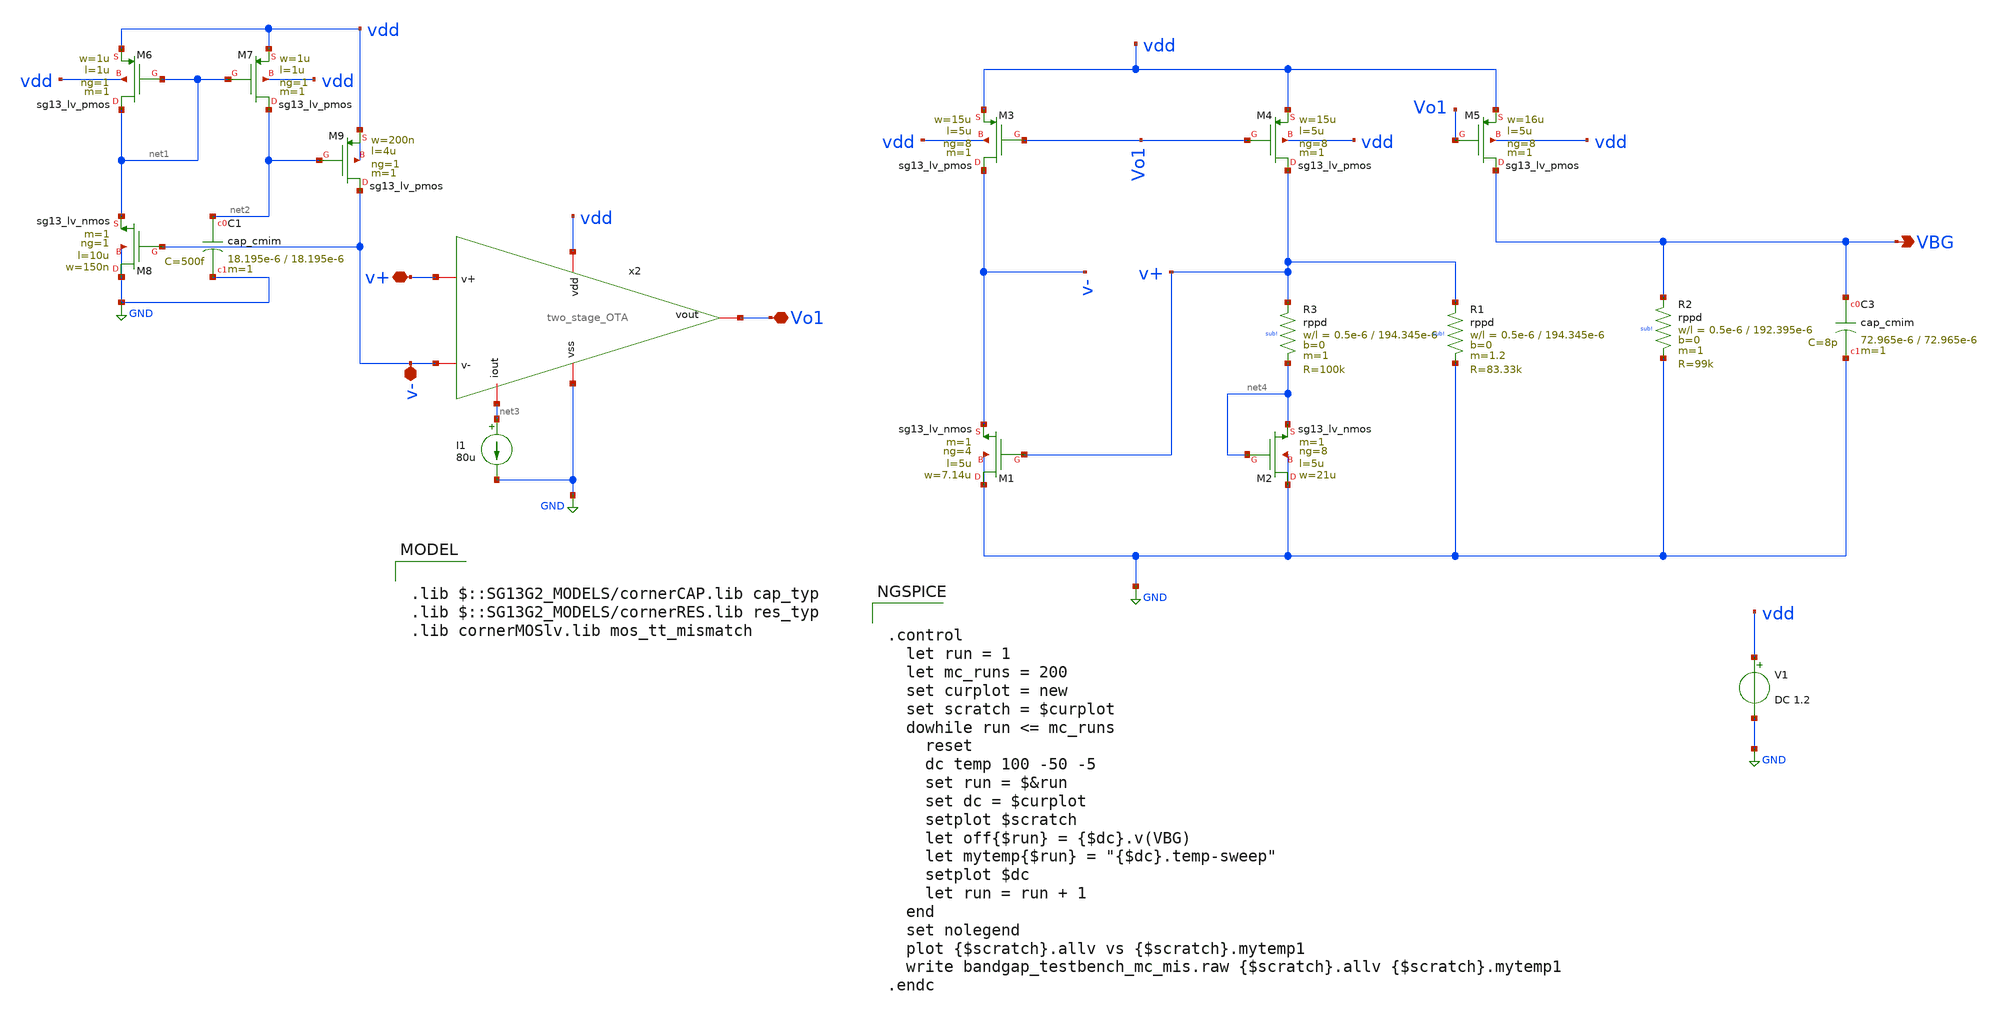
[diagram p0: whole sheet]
** sch_path: modules/module_1_bandgap_reference/part_2_full_bgr/schematic/bandgap_MC.sch
**.subckt bandgap_MC v+ v- Vo1 VBG
*.iopin v+
*.iopin v-
*.iopin Vo1
*.opin VBG
XM8 GND v- net1 GND sg13_lv_nmos w=150n l=10u ng=1 m=1 mm_ok=1
XM6 net1 net1 vdd vdd sg13_lv_pmos w=1u l=1u ng=1 m=1 mm_ok=1
XM7 net2 net1 vdd vdd sg13_lv_pmos w=1u l=1u ng=1 m=1 mm_ok=1
XM9 v- net2 vdd vdd sg13_lv_pmos w=200n l=4u ng=1 m=1 mm_ok=1
x2 vdd net3 v+ v- Vo1 GND two_stage_OTA
I1 net3 GND 80u
V1 vdd GND DC 1.2
XM1 GND v+ v- GND sg13_lv_nmos w=7.14u l=5u ng=4 m=1 mm_ok=1
XM2 GND net4 net4 GND sg13_lv_nmos w=21u l=5u ng=8 m=1 mm_ok=1
XM3 v- Vo1 vdd vdd sg13_lv_pmos w=15u l=5u ng=8 m=1 mm_ok=1
XM4 v+ Vo1 vdd vdd sg13_lv_pmos w=15u l=5u ng=8 m=1 mm_ok=1
XM5 VBG Vo1 vdd vdd sg13_lv_pmos w=16u l=5u ng=8 m=1 mm_ok=1
XC3 VBG GND cap_cmim w=72.965e-6 l=72.965e-6 m=1 mm_ok=1
XR3 v+ net4 sub! rppd w=0.5e-6 l=194.345e-6 m=1 b=0 mm_ok=1
XR1 v+ GND sub! rppd w=0.5e-6 l=194.345e-6 m=1.2 b=0 mm_ok=1
XR2 VBG GND sub! rppd w=0.5e-6 l=192.395e-6 m=1 b=0 mm_ok=1
XC1 net2 GND cap_cmim w=18.195e-6 l=18.195e-6 m=1 mm_ok=1
**** begin user architecture code


.control
  let run = 1
  let mc_runs = 200
  set curplot = new
  set scratch = $curplot
  dowhile run <= mc_runs
    reset
    dc temp 100 -50 -5
    set run = $&run
    set dc = $curplot
    setplot $scratch
    let off{$run} = {$dc}.v(VBG)
    let mytemp{$run} = "{$dc}.temp-sweep"
    setplot $dc
    let run = run + 1
  end
  set nolegend
  plot {$scratch}.allv vs {$scratch}.mytemp1
  write bandgap_testbench_mc_mis.raw {$scratch}.allv {$scratch}.mytemp1
.endc




.lib $::SG13G2_MODELS/cornerCAP.lib cap_typ
.lib $::SG13G2_MODELS/cornerRES.lib res_typ
.lib cornerMOSlv.lib mos_tt_mismatch

**** end user architecture code
**.ends

* expanding   symbol:
*+  /home/pedersen/projects/IHP-AnalogAcademy/modules/module_1_bandgap_reference/part_1_OTA/schematic/two_stage_OTA.sym # of pins=6
** sym_path: /home/pedersen/projects/IHP-AnalogAcademy/modules/module_1_bandgap_reference/part_1_OTA/schematic/two_stage_OTA.sym
** sch_path: /home/pedersen/projects/IHP-AnalogAcademy/modules/module_1_bandgap_reference/part_1_OTA/schematic/two_stage_OTA.sch
.subckt two_stage_OTA vdd iout v+ v- vout vss
*.iopin v-
*.iopin v+
*.iopin vss
*.iopin vdd
*.iopin iout
*.iopin vout
XM4 vss net1 net3 vss sg13_lv_nmos w=720n l=9.75u ng=1 m=1 mm_ok=1
XM3 vss net1 net1 vss sg13_lv_nmos w=720n l=9.75u ng=1 m=1 mm_ok=1
XM1 net1 v- net2 vdd sg13_lv_pmos w=7.41u l=3.64u ng=1 m=1 mm_ok=1
XM2 net3 v+ net2 vdd sg13_lv_pmos w=7.41u l=3.64u ng=1 m=1 mm_ok=1
XM5 net2 iout vdd vdd sg13_lv_pmos w=5.3u l=1.95u ng=1 m=1 mm_ok=1
XM7 vout iout vdd vdd sg13_lv_pmos w=75u l=2.08u ng=8 m=1 mm_ok=1
XM6 vss net3 vout vss sg13_lv_nmos w=28.8u l=9.75u ng=4 m=1 mm_ok=1
XM9 iout iout vdd vdd sg13_lv_pmos w=75u l=2.08u ng=8 m=1 mm_ok=1
XC2 net3 vout cap_cmim w=22.295e-6 l=22.295e-6 m=1 mm_ok=1
.ends

.GLOBAL GND
.end
